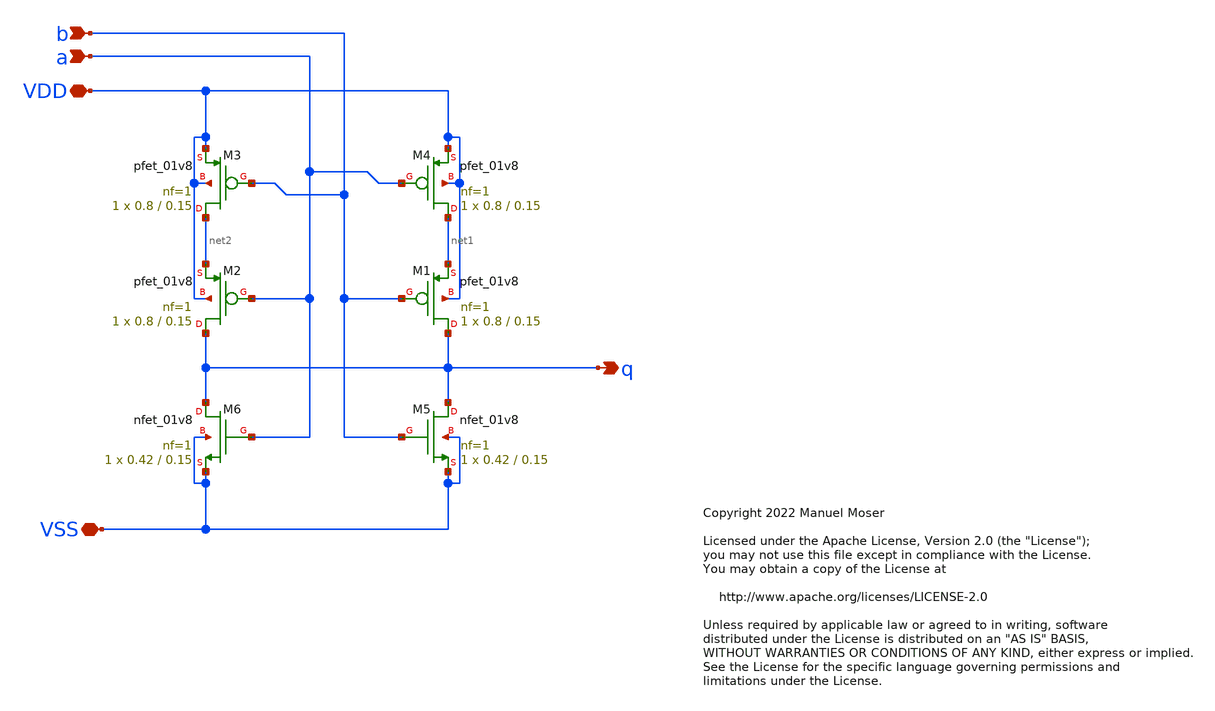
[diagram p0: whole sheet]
** sch_path: xschem/adc_nor.sch
* Copyright 2022 Manuel Moser
* Licensed under the Apache License, Version 2.0 (the "License");
**.subckt adc_nor VDD VSS b a q
*.iopin VDD
*.iopin VSS
*.ipin b
*.ipin a
*.opin q
XM5 q b VSS VSS sky130_fd_pr__nfet_01v8 L=0.15 W=0.42 nf=1 ad='int((nf+1)/2) * W/nf * 0.29' as='int((nf+2)/2) * W/nf * 0.29'
+ pd='2*int((nf+1)/2) * (W/nf + 0.29)' ps='2*int((nf+2)/2) * (W/nf + 0.29)' nrd='0.29 / W' nrs='0.29 / W'
+ sa=0 sb=0 sd=0 mult=1 m=1
XM6 q a VSS VSS sky130_fd_pr__nfet_01v8 L=0.15 W=0.42 nf=1 ad='int((nf+1)/2) * W/nf * 0.29' as='int((nf+2)/2) * W/nf * 0.29'
+ pd='2*int((nf+1)/2) * (W/nf + 0.29)' ps='2*int((nf+2)/2) * (W/nf + 0.29)' nrd='0.29 / W' nrs='0.29 / W'
+ sa=0 sb=0 sd=0 mult=1 m=1
XM1 q b net1 VDD sky130_fd_pr__pfet_01v8 L=0.15 W=0.8 nf=1 ad='int((nf+1)/2) * W/nf * 0.29' as='int((nf+2)/2) * W/nf * 0.29'
+ pd='2*int((nf+1)/2) * (W/nf + 0.29)' ps='2*int((nf+2)/2) * (W/nf + 0.29)' nrd='0.29 / W' nrs='0.29 / W'
+ sa=0 sb=0 sd=0 mult=1 m=1
XM2 q a net2 VDD sky130_fd_pr__pfet_01v8 L=0.15 W=0.8 nf=1 ad='int((nf+1)/2) * W/nf * 0.29' as='int((nf+2)/2) * W/nf * 0.29'
+ pd='2*int((nf+1)/2) * (W/nf + 0.29)' ps='2*int((nf+2)/2) * (W/nf + 0.29)' nrd='0.29 / W' nrs='0.29 / W'
+ sa=0 sb=0 sd=0 mult=1 m=1
XM3 net2 b VDD VDD sky130_fd_pr__pfet_01v8 L=0.15 W=0.8 nf=1 ad='int((nf+1)/2) * W/nf * 0.29' as='int((nf+2)/2) * W/nf * 0.29'
+ pd='2*int((nf+1)/2) * (W/nf + 0.29)' ps='2*int((nf+2)/2) * (W/nf + 0.29)' nrd='0.29 / W' nrs='0.29 / W'
+ sa=0 sb=0 sd=0 mult=1 m=1
XM4 net1 a VDD VDD sky130_fd_pr__pfet_01v8 L=0.15 W=0.8 nf=1 ad='int((nf+1)/2) * W/nf * 0.29' as='int((nf+2)/2) * W/nf * 0.29'
+ pd='2*int((nf+1)/2) * (W/nf + 0.29)' ps='2*int((nf+2)/2) * (W/nf + 0.29)' nrd='0.29 / W' nrs='0.29 / W'
+ sa=0 sb=0 sd=0 mult=1 m=1
**.ends
.end
